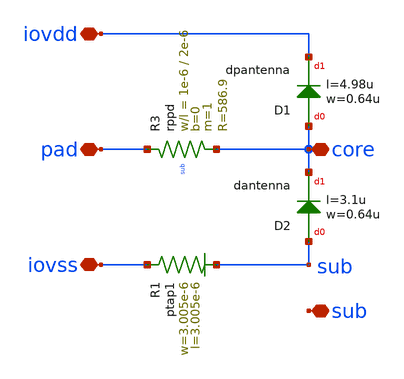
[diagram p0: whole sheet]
** sch_path: MSPHY6034-main/schematic/xschem/openpdk-libraries/ihp-sg13g2/sg13g2_io/xschem/sg13g2_SecondaryProtection.sch
**.subckt sg13g2_SecondaryProtection iovss core pad iovdd sub
*.iopin iovss
*.iopin core
*.iopin pad
*.iopin iovdd
*.iopin sub
XR1 iovss sub ptap1 R=46.56 w=3.005e-6 l=3.005e-6
XD1 core iovdd dpantenna l=4.98u w=0.64u
XD2 sub core dantenna l=3.1u w=0.64u
XR3 pad core sub rppd w=1e-6 l=2e-6 m=1 b=0 mm_ok=1
**.ends
.end
